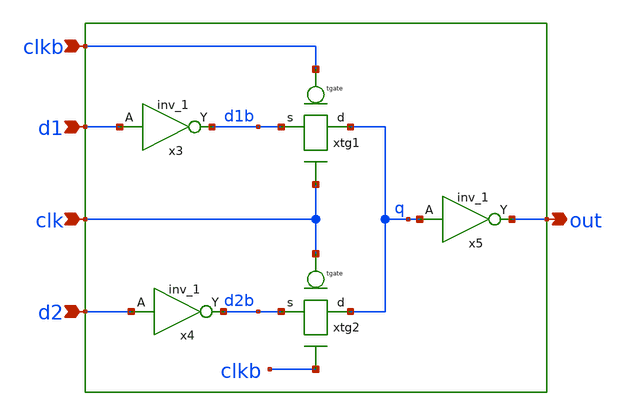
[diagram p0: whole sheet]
** sch_path: src/xe/test_cases/mux.sch
**.subckt mux d1 d2 out clkb clk
*.ipin d1
*.ipin d2
*.opin out
*.ipin clkb
*.ipin clk
xtg1 clkb d1b q clk vcc vss tgate
xtg2 clk d2b q clkb vcc vss tgate
x3 d1 vss vss vcc vcc d1b sky130_fd_sc_hd__inv_1
x4 d2 vss vss vcc vcc d2b sky130_fd_sc_hd__inv_1
x5 q vss vss vcc vcc out sky130_fd_sc_hd__inv_1
**.ends

* expanding   symbol:  yxt/tgate.sym # of pins=4
** sym_path: src/xe/test_cases/tgate.sym
** sch_path: src/xe/test_cases/tgate.sch
.subckt tgate gp s d gn vcc vss
*.ipin s
*.ipin gp
*.ipin gn
*.opin d
XMpc d gp s vss sky130_fd_pr__pfet_01v8 L=0.15 W=1 nf=1 ad='int((nf+1)/2) * W/nf * 0.29' as='int((nf+2)/2) * W/nf * 0.29'
+ pd='2*int((nf+1)/2) * (W/nf + 0.29)' ps='2*int((nf+2)/2) * (W/nf + 0.29)' nrd='0.29 / W' nrs='0.29 / W'
+ sa=0 sb=0 sd=0 mult=7 m=7
XM15 s gn d vcc sky130_fd_pr__nfet_01v8 L=0.15 W=1 nf=1 ad='int((nf+1)/2) * W/nf * 0.29' as='int((nf+2)/2) * W/nf * 0.29'
+ pd='2*int((nf+1)/2) * (W/nf + 0.29)' ps='2*int((nf+2)/2) * (W/nf + 0.29)' nrd='0.29 / W' nrs='0.29 / W'
+ sa=0 sb=0 sd=0 mult=1 m=1
.ends

.end
